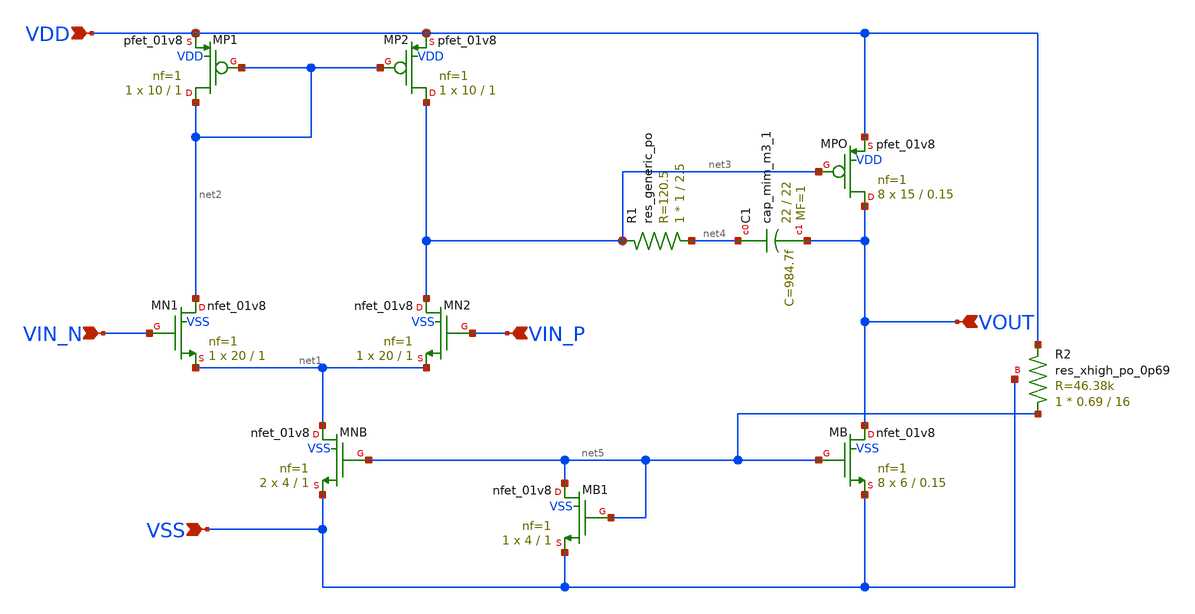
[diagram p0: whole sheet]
** sch_path: analog/bootcamp_opamp/schematics/opamp_two_stage.sch
**.subckt opamp_two_stage VIN_N VIN_P VDD VSS VOUT
*.ipin VIN_N
*.ipin VIN_P
*.ipin VDD
*.ipin VSS
*.ipin VOUT
XMN1 net2 VIN_N net1 VSS sky130_fd_pr__nfet_01v8 L=1 W=20 nf=1 ad='int((nf+1)/2) * W/nf * 0.29' as='int((nf+2)/2) * W/nf * 0.29'
+ pd='2*int((nf+1)/2) * (W/nf + 0.29)' ps='2*int((nf+2)/2) * (W/nf + 0.29)' nrd='0.29 / W' nrs='0.29 / W'
+ sa=0 sb=0 sd=0 mult=1 m=1
XMP1 net2 net2 VDD VDD sky130_fd_pr__pfet_01v8 L=1 W=10 nf=1 ad='int((nf+1)/2) * W/nf * 0.29' as='int((nf+2)/2) * W/nf * 0.29'
+ pd='2*int((nf+1)/2) * (W/nf + 0.29)' ps='2*int((nf+2)/2) * (W/nf + 0.29)' nrd='0.29 / W' nrs='0.29 / W'
+ sa=0 sb=0 sd=0 mult=1 m=1
XMP2 net3 net2 VDD VDD sky130_fd_pr__pfet_01v8 L=1 W=10 nf=1 ad='int((nf+1)/2) * W/nf * 0.29' as='int((nf+2)/2) * W/nf * 0.29'
+ pd='2*int((nf+1)/2) * (W/nf + 0.29)' ps='2*int((nf+2)/2) * (W/nf + 0.29)' nrd='0.29 / W' nrs='0.29 / W'
+ sa=0 sb=0 sd=0 mult=1 m=1
XMN2 net3 VIN_P net1 VSS sky130_fd_pr__nfet_01v8 L=1 W=20 nf=1 ad='int((nf+1)/2) * W/nf * 0.29' as='int((nf+2)/2) * W/nf * 0.29'
+ pd='2*int((nf+1)/2) * (W/nf + 0.29)' ps='2*int((nf+2)/2) * (W/nf + 0.29)' nrd='0.29 / W' nrs='0.29 / W'
+ sa=0 sb=0 sd=0 mult=1 m=1
XMNB net1 net5 VSS VSS sky130_fd_pr__nfet_01v8 L=1 W=4 nf=1 ad='int((nf+1)/2) * W/nf * 0.29' as='int((nf+2)/2) * W/nf * 0.29'
+ pd='2*int((nf+1)/2) * (W/nf + 0.29)' ps='2*int((nf+2)/2) * (W/nf + 0.29)' nrd='0.29 / W' nrs='0.29 / W'
+ sa=0 sb=0 sd=0 mult=2 m=2
XMPO VOUT net3 VDD VDD sky130_fd_pr__pfet_01v8 L=0.15 W=15 nf=1 ad='int((nf+1)/2) * W/nf * 0.29' as='int((nf+2)/2) * W/nf * 0.29'
+ pd='2*int((nf+1)/2) * (W/nf + 0.29)' ps='2*int((nf+2)/2) * (W/nf + 0.29)' nrd='0.29 / W' nrs='0.29 / W'
+ sa=0 sb=0 sd=0 mult=8 m=8
XR1 net4 net3 sky130_fd_pr__res_generic_po W=1 L=2.5 m=1
XC1 net4 VOUT sky130_fd_pr__cap_mim_m3_1 W=22 L=22 MF=1 m=1
XMB VOUT net5 VSS VSS sky130_fd_pr__nfet_01v8 L=0.15 W=6 nf=1 ad='int((nf+1)/2) * W/nf * 0.29' as='int((nf+2)/2) * W/nf * 0.29'
+ pd='2*int((nf+1)/2) * (W/nf + 0.29)' ps='2*int((nf+2)/2) * (W/nf + 0.29)' nrd='0.29 / W' nrs='0.29 / W'
+ sa=0 sb=0 sd=0 mult=8 m=8
XR2 net5 VDD VSS sky130_fd_pr__res_xhigh_po_0p69 L=16 mult=1 m=1
XMB1 net5 net5 VSS VSS sky130_fd_pr__nfet_01v8 L=1 W=4 nf=1 ad='int((nf+1)/2) * W/nf * 0.29' as='int((nf+2)/2) * W/nf * 0.29'
+ pd='2*int((nf+1)/2) * (W/nf + 0.29)' ps='2*int((nf+2)/2) * (W/nf + 0.29)' nrd='0.29 / W' nrs='0.29 / W'
+ sa=0 sb=0 sd=0 mult=1 m=1
**.ends
.end
